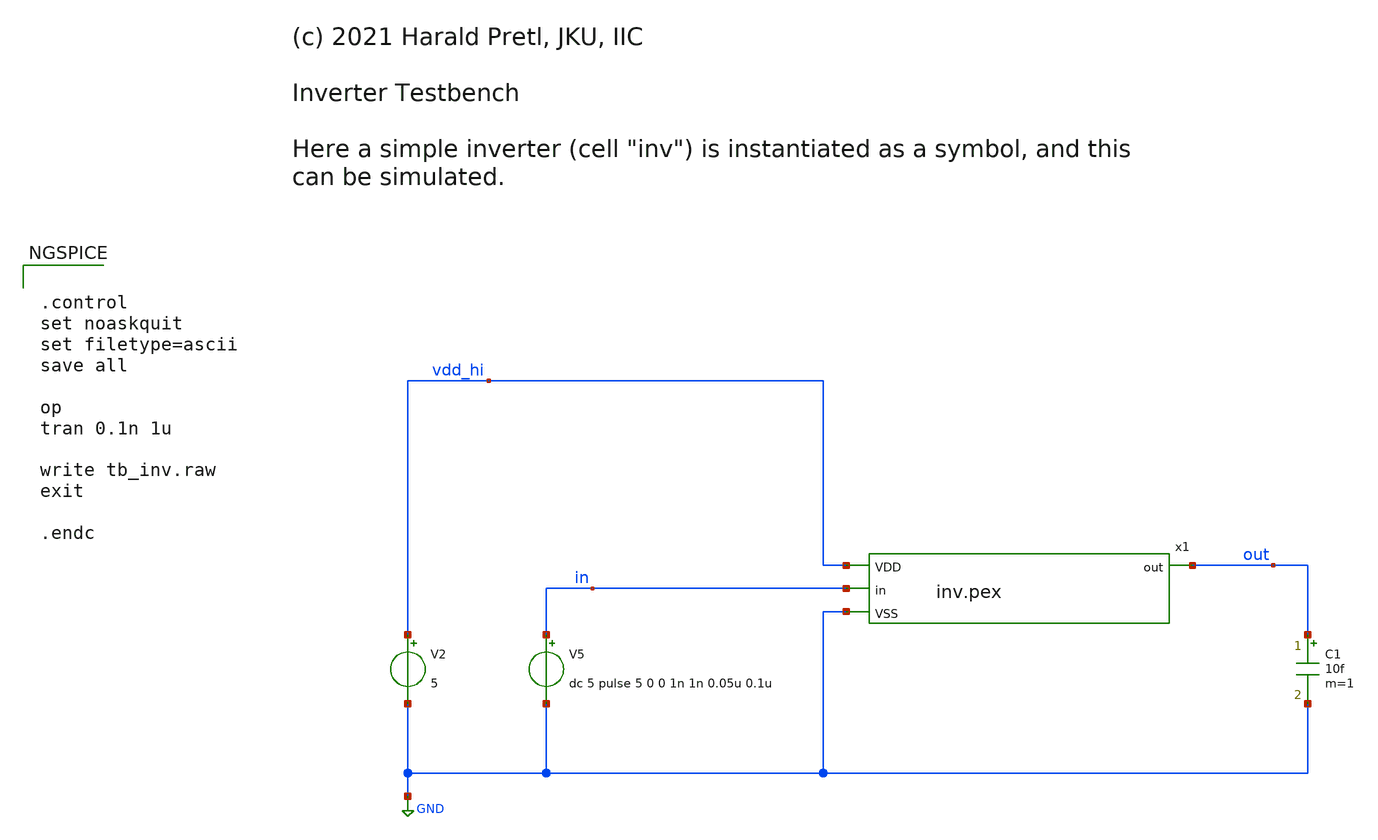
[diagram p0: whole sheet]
** sch_path: example/ana/tb_inv_pex.sch
* (c) 2021 Harald Pretl, JKU, IIC
**.subckt tb_inv_pex
V2 vdd_hi GND 5
V5 in GND dc 5 pulse 5 0 0 1n 1n 0.05u 0.1u
x1 vdd_hi in out GND inv.pex
C1 out GND 10f m=1
**** begin user architecture code
 ** manual skywater pdks install (with patches applied)
* .lib $::SKYWATER_MODELS/models/sky130.lib.spice tt

** opencircuitdesign pdks install
.lib $::SKYWATER_MODELS/sky130.lib.spice.tt.red tt

.param mc_mm_switch=0
.param mc_pr_switch=0



.control
set noaskquit
set filetype=ascii
save all

op
tran 0.1n 1u

write tb_inv.raw
exit

.endc


**** end user architecture code
**.ends

* expanding   symbol:  inv.pex.sym # of pins=4
** sym_path: example/ana/inv.pex.sym
** sch_path: example/ana/inv.pex.sch
.subckt inv.pex VDD in out VSS
*.ipin in
*.opin out
*.ipin VDD
*.ipin VSS
* noconn out
* noconn VDD
* noconn in
* noconn VSS
**** begin user architecture code

.include inv.pex.spice

**** end user architecture code
.ends

.GLOBAL GND
.end
